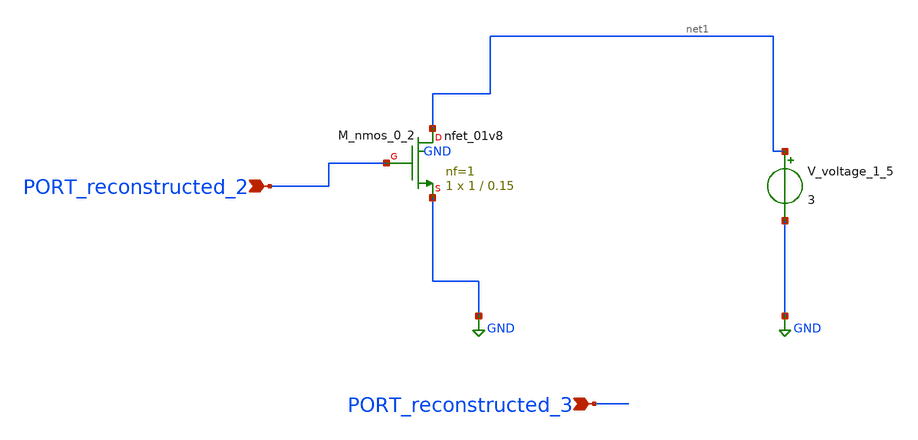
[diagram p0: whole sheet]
** sch_path: schematics/AMSNet/11.sch
**.subckt 11 PORT_reconstructed_2 PORT_reconstructed_3
*.ipin PORT_reconstructed_2
*.ipin PORT_reconstructed_3
XM_nmos_0_2 net1 PORT_reconstructed_2 GND GND sky130_fd_pr__nfet_01v8 L=0.15 W=1 nf=1 ad='int((1 + 1)/2) * 1 / 1 * 0.29'
+ as='int((1 + 2)/2) * 1 / 1 * 0.29' pd='2*int((1 + 1)/2) * (1 / 1 + 0.29)' ps='2*int((1 + 2)/2) * (1 / 1 + 0.29)'
+ nrd='0.29 / 1 ' nrs='0.29 / 1 ' sa=0 sb=0 sd=0 mult=1 m=1
V_voltage_1_5 net1 GND 3
**.ends
.GLOBAL GND
.end
